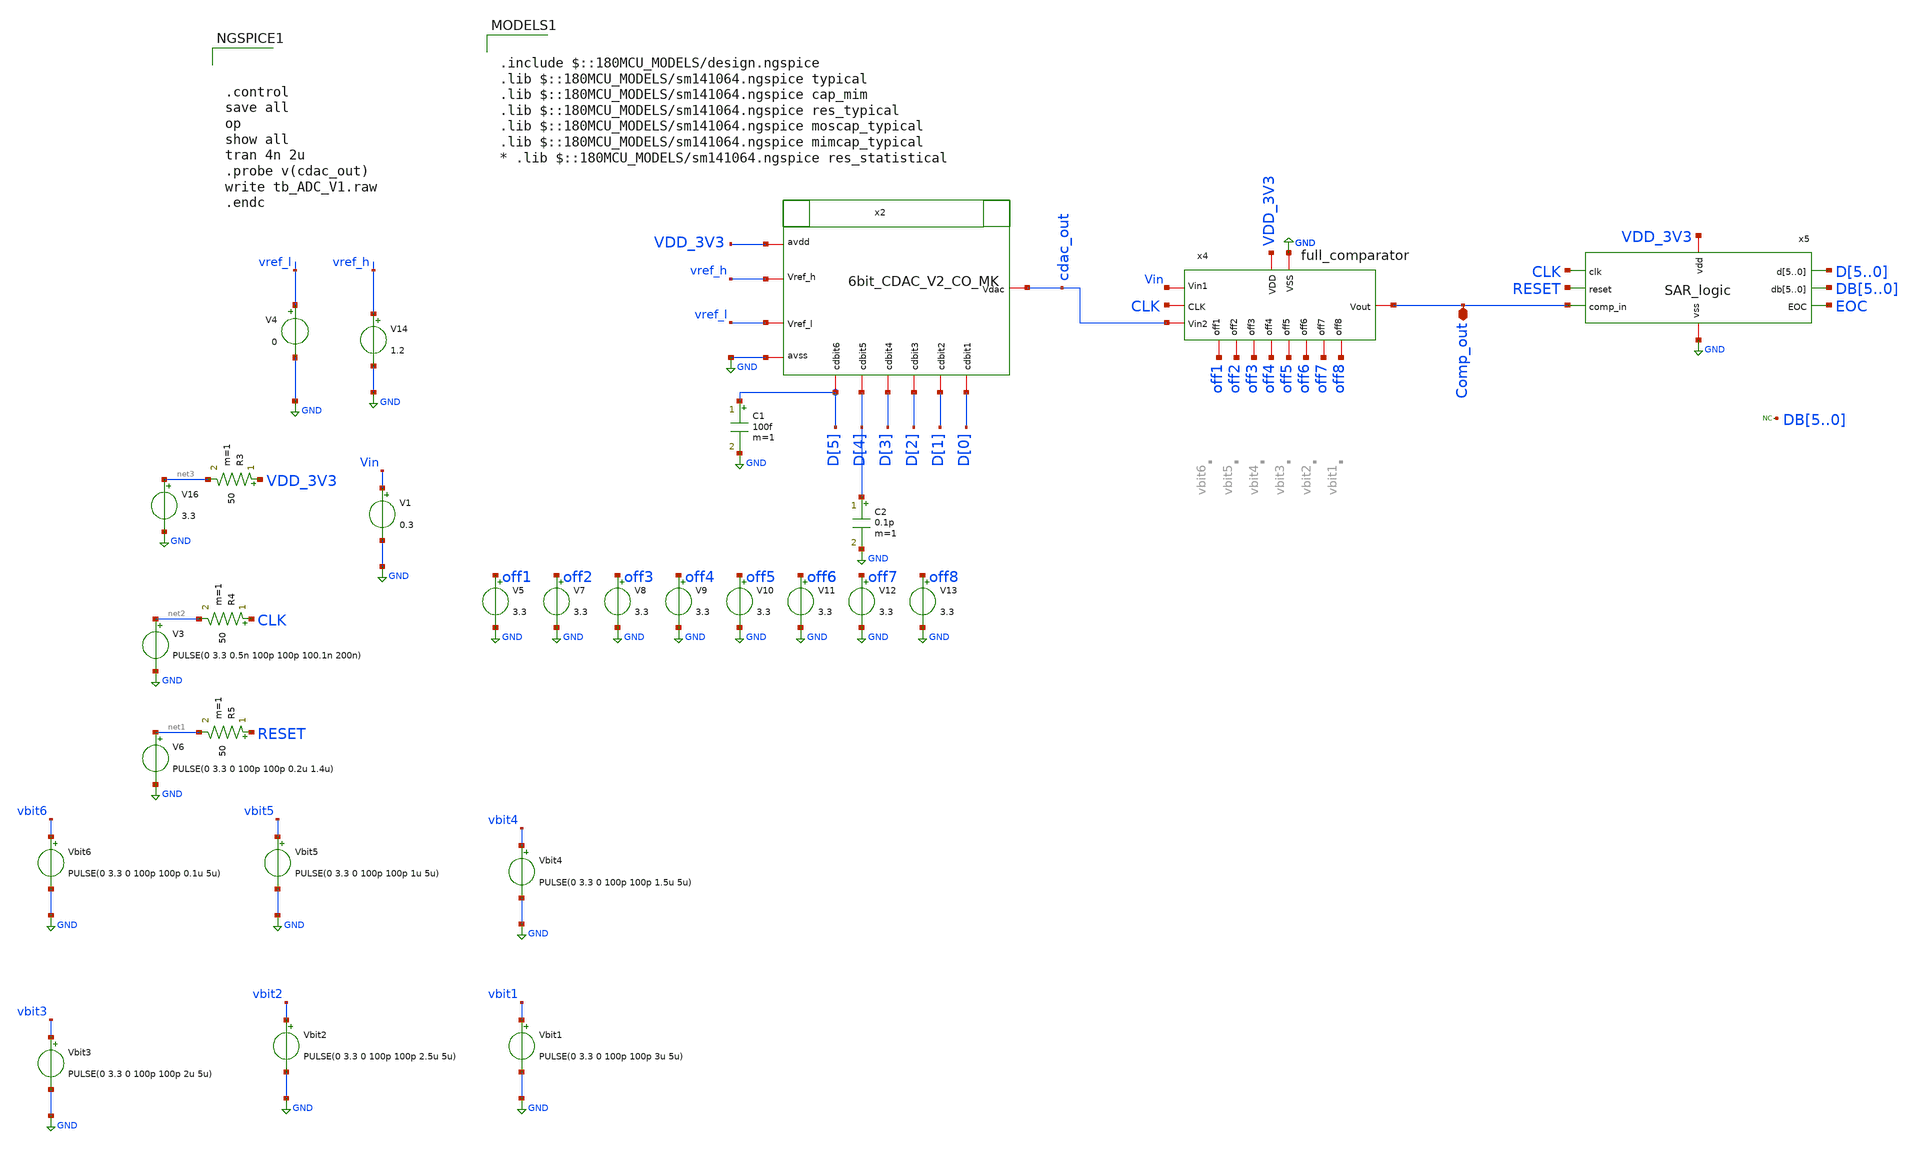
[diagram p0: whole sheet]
** sch_path: designs/full_ADC/TB_ADC_V1.sch
**.subckt TB_ADC_V1 Comp_out
*.iopin Comp_out
V14 vref_h GND 1.2
V5 off1 GND 3.3
V7 off2 GND 3.3
V8 off3 GND 3.3
V9 off4 GND 3.3
V10 off5 GND 3.3
V11 off6 GND 3.3
V12 off7 GND 3.3
V13 off8 GND 3.3
V6 net1 GND PULSE(0 3.3 0 100p 100p 0.2u 1.4u)
R5 RESET net1 50 m=1
x4 off1 VDD_3V3 GND off2 CLK off3 Vin off4 cdac_out off5 Comp_out off6 off7 off8 full_comparator
x5 VDD_3V3 GND CLK RESET Comp_out D5 D4 D3 D2 D1 D0 DB5 DB4 DB3 DB2 DB1 DB0 EOC SAR_logic
V1 Vin GND 0.3
V3 net2 GND PULSE(0 3.3 0.5n 100p 100p 100.1n 200n)
R4 CLK net2 50 m=1
x2 vref_l cdac_out VDD_3V3 GND vref_h D[5] D[4] D[2] D[0] D[1] D[3] 6bit_CDAC_V2_CO_MK
V4 vref_l GND 0
V16 net3 GND 3.3
R3 VDD_3V3 net3 50 m=1
* noconn DB[5..0]
Vbit1 vbit1 GND PULSE(0 3.3 0 100p 100p 3u 5u)
Vbit2 vbit2 GND PULSE(0 3.3 0 100p 100p 2.5u 5u)
Vbit3 vbit3 GND PULSE(0 3.3 0 100p 100p 2u 5u)
Vbit4 vbit4 GND PULSE(0 3.3 0 100p 100p 1.5u 5u)
Vbit5 vbit5 GND PULSE(0 3.3 0 100p 100p 1u 5u)
Vbit6 vbit6 GND PULSE(0 3.3 0 100p 100p 0.1u 5u)
C1 D[5] GND 100f m=1
C2 D[4] GND 0.1p m=1
**** begin user architecture code



.control
save all
op
show all
tran 4n 2u
.probe v(cdac_out)
write tb_ADC_V1.raw
.endc



.include $::180MCU_MODELS/design.ngspice
.lib $::180MCU_MODELS/sm141064.ngspice typical
.lib $::180MCU_MODELS/sm141064.ngspice cap_mim
.lib $::180MCU_MODELS/sm141064.ngspice res_typical
.lib $::180MCU_MODELS/sm141064.ngspice moscap_typical
.lib $::180MCU_MODELS/sm141064.ngspice mimcap_typical
* .lib $::180MCU_MODELS/sm141064.ngspice res_statistical

**** end user architecture code
**.ends
.GLOBAL GND
.end
